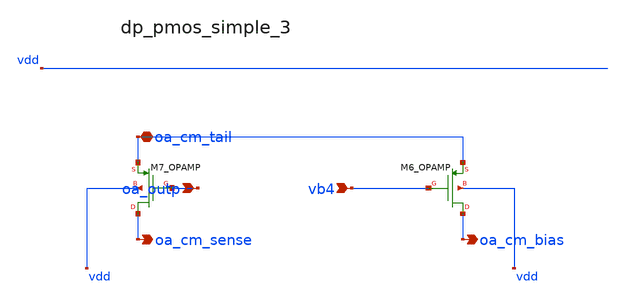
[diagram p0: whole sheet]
** sch_path: analog-db/raw/sup_003_rrl_sc_integrator/hier/blocks/dp_pmos_simple_3.sch
**.subckt dp_pmos_simple_3 oa_outp vb4 oa_cm_tail oa_cm_sense oa_cm_bias
*.ipin oa_outp
*.ipin vb4
*.iopin oa_cm_tail
*.opin oa_cm_sense
*.opin oa_cm_bias
XM6_OPAMP oa_cm_bias vb4 oa_cm_tail vdd sg13_lv_pmos w=x_dut_xm6_opamp_w l=x_dut_xm6_opamp_l ng=1
+ m=x_dut_xm6_opamp_m
XM7_OPAMP oa_cm_sense oa_outp oa_cm_tail vdd sg13_lv_pmos w=x_dut_xm7_opamp_w l=x_dut_xm7_opamp_l
+ ng=1 m=x_dut_xm7_opamp_m
**.ends
.end
